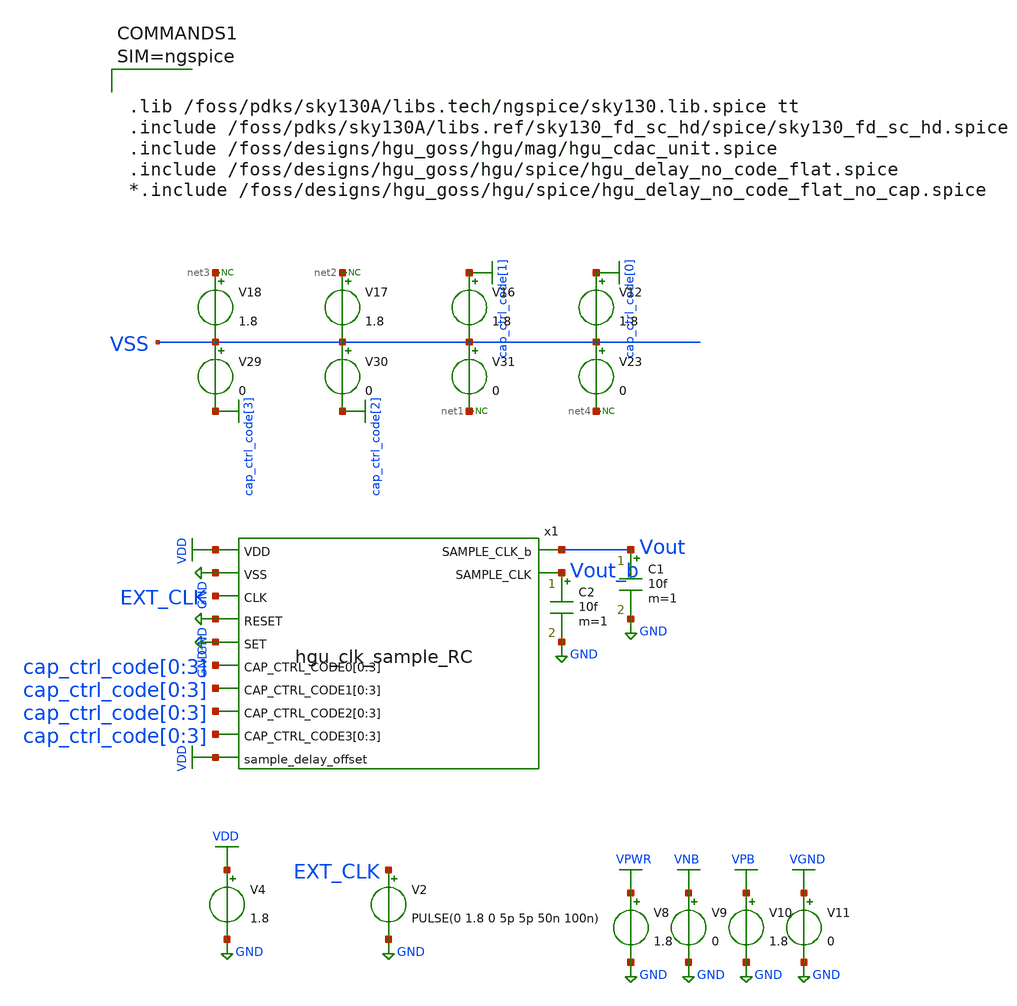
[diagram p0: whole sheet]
** sch_path: hgu/tb/tb_hgu_clk_sample.sch
**.subckt tb_hgu_clk_sample
V2 EXT_CLK GND PULSE(0 1.8 0 5p 5p 50n 100n)
V4 VDD GND 1.8
x1 Vout VDD GND EXT_CLK GND GND Vout_b cap_ctrl_code[0] cap_ctrl_code[1] cap_ctrl_code[2]
+ cap_ctrl_code[3] cap_ctrl_code[0] cap_ctrl_code[1] cap_ctrl_code[2] cap_ctrl_code[3] cap_ctrl_code[0]
+ cap_ctrl_code[1] cap_ctrl_code[2] cap_ctrl_code[3] cap_ctrl_code[0] cap_ctrl_code[1] cap_ctrl_code[2]
+ cap_ctrl_code[3] VDD hgu_clk_sample_RC
C1 Vout GND 10f m=1
V8 VPWR GND 1.8
V9 VNB GND 0
V10 VPB GND 1.8
V11 VGND GND 0
V12 cap_ctrl_code[0] VSS 1.8
V29 VSS cap_ctrl_code[3] 0
V30 VSS cap_ctrl_code[2] 0
V31 VSS net1 0
V16 cap_ctrl_code[1] VSS 1.8
V17 net2 VSS 1.8
V18 net3 VSS 1.8
V23 VSS net4 0
* noconn #net3
* noconn #net2
* noconn #net1
* noconn #net4
C2 Vout_b GND 10f m=1
**** begin user architecture code





.tran 10ps 200ns

.control
	option temp = 0
	let vdd_act = 1.98

	alter V1 vdd_act

	run
	plot V(Vout) V(Vout_b) V(EXT_CLK)+2

	let l_vdd = vdd_act * 0.2
        let h_vdd = vdd_act * 0.8
        let m_vdd = vdd_act * 0.5
        meas tran rising_s find time when V(Vout)=l_vdd RISE=1 TD=90n
        meas tran rising_e find time when V(Vout)=h_vdd RISE=1 TD=90n
        let rising_time = rising_e-rising_s
        meas tran falling_s find time when V(Vout)=h_vdd FALL=1 TD=90n
        meas tran falling_e find time when V(Vout)=l_vdd FALL=1 TD=90n
        let falling_time = falling_e-falling_s
        meas tran IN find time when V(ext_clk)=m_vdd RISE=1 TD=90n
        meas tran OUT find time when V(Vout)=m_vdd RISE=1 TD=90n
        let rising_delay = OUT-IN

	meas tran IN find time when V(Vout)=m_vdd RISE=1 TD=90n
        meas tran OUT find time when V(Vout)=m_vdd FALL=1 TD=90n
        let on_time = OUT-IN

	print rising_time falling_time rising_delay on_time
.endc
.save all






.lib /foss/pdks/sky130A/libs.tech/ngspice/sky130.lib.spice tt
.include /foss/pdks/sky130A/libs.ref/sky130_fd_sc_hd/spice/sky130_fd_sc_hd.spice
.include /foss/designs/hgu_goss/hgu/mag/hgu_cdac_unit.spice
.include /foss/designs/hgu_goss/hgu/spice/hgu_delay_no_code_flat.spice
*.include /foss/designs/hgu_goss/hgu/spice/hgu_delay_no_code_flat_no_cap.spice



**** end user architecture code
**.ends
.GLOBAL GND
.GLOBAL VDD
.GLOBAL VGND
.GLOBAL VNB
.GLOBAL VPB
.GLOBAL VPWR
.GLOBAL cap_ctrl_code[3]
.GLOBAL cap_ctrl_code[2]
.GLOBAL cap_ctrl_code[1]
.GLOBAL cap_ctrl_code[0]
.end
